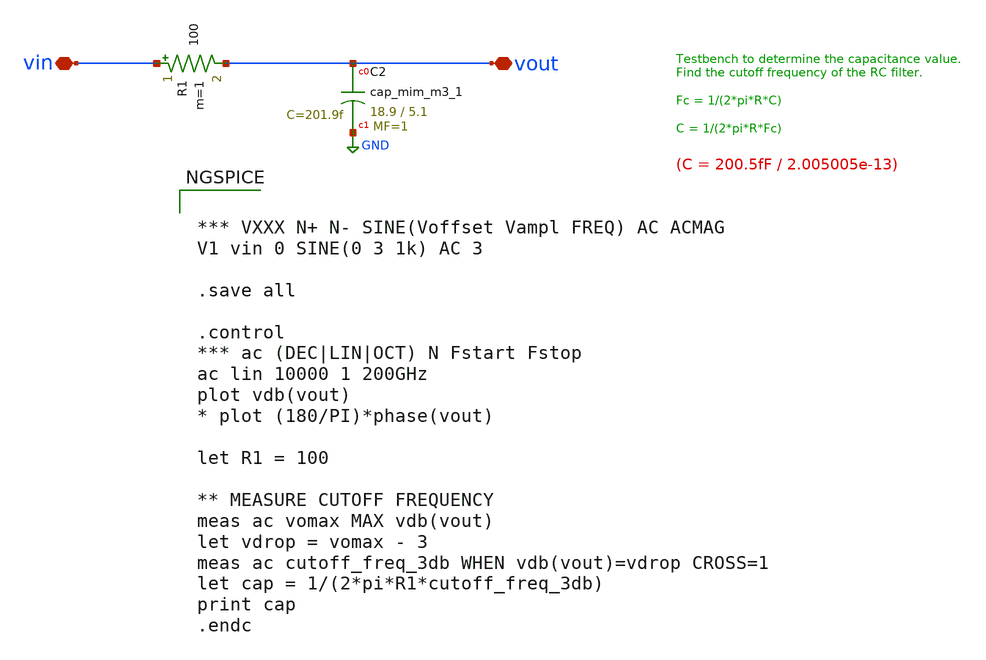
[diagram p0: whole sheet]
** sch_path: testdata/designs/sky130A/cap_mim_m3_w18p9_l5p1_no_interconnect/cap_mim_m3_w18p9_l5p1_tb.sch
**.subckt cap_mim_m3_w18p9_l5p1_tb vin vout
*.iopin vin
*.iopin vout
R1 vin vout 100 m=1
XC2 vout GND sky130_fd_pr__cap_mim_m3_1 W=18.9 L=5.1 MF=1 m=1
**** begin user architecture code


*** VXXX N+ N- SINE(Voffset Vampl FREQ) AC ACMAG
V1 vin 0 SINE(0 3 1k) AC 3

.save all

.control
*** ac (DEC|LIN|OCT) N Fstart Fstop
ac lin 10000 1 200GHz
plot vdb(vout)
* plot (180/PI)*phase(vout)

let R1 = 100

** MEASURE CUTOFF FREQUENCY
meas ac vomax MAX vdb(vout)
let vdrop = vomax - 3
meas ac cutoff_freq_3db WHEN vdb(vout)=vdrop CROSS=1
let cap = 1/(2*pi*R1*cutoff_freq_3db)
print cap
.endc



** opencircuitdesign pdks install
.lib $::SKYWATER_MODELS/sky130.lib.spice tt


**** end user architecture code
**.ends
.GLOBAL GND
.end
